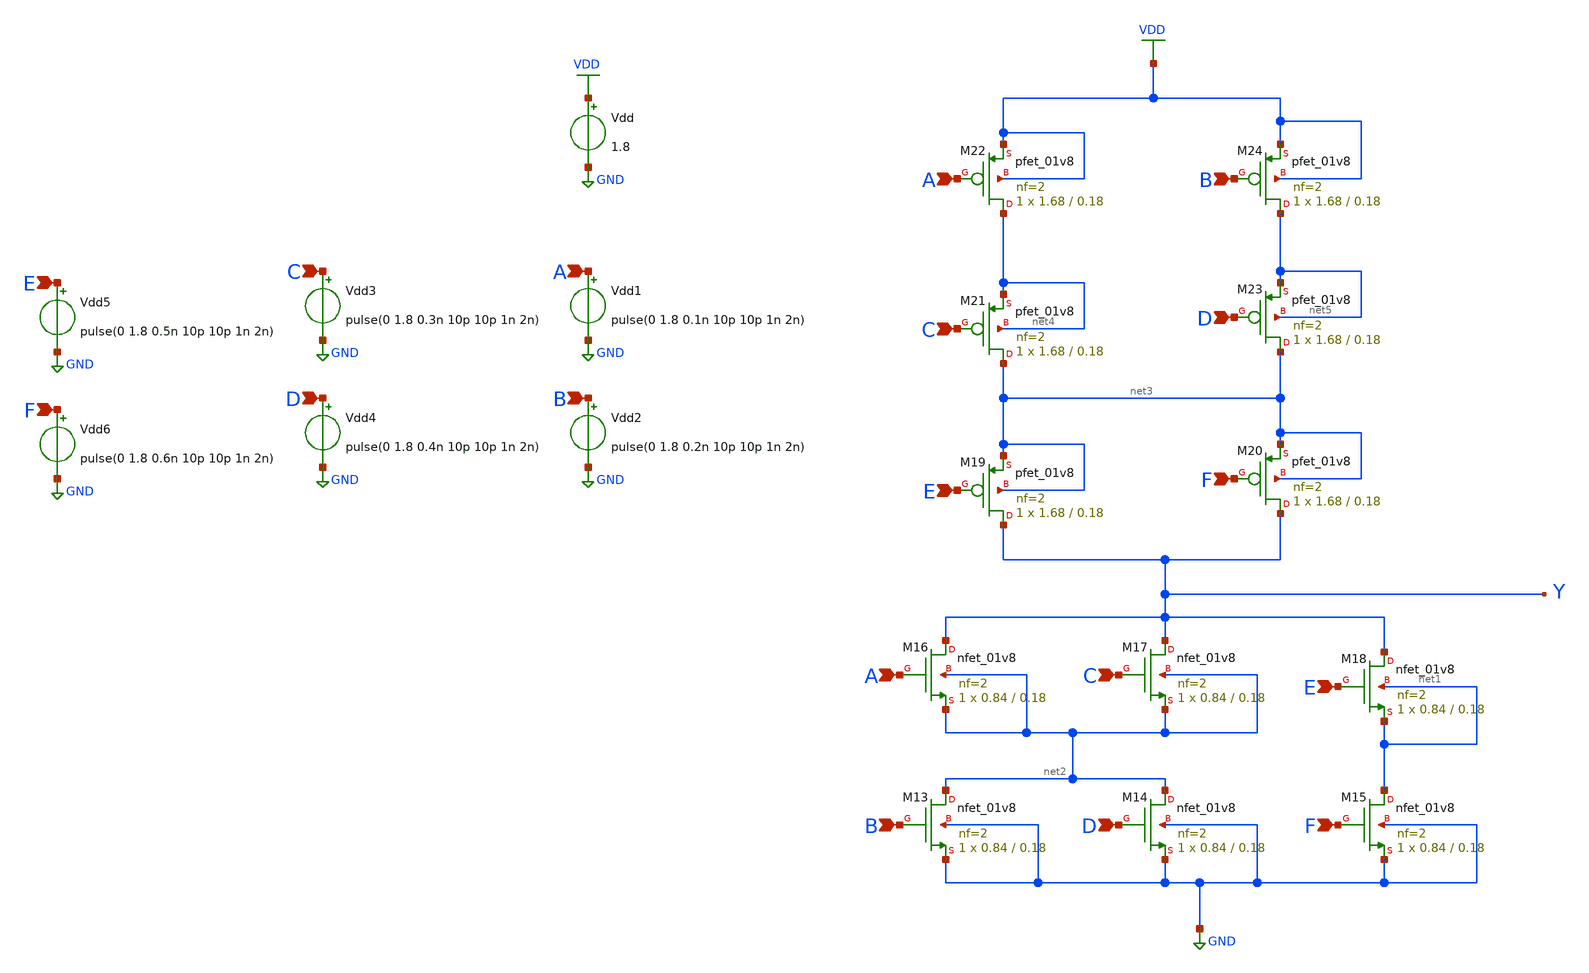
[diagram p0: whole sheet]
** sch_path: Week 1/xschem 840_1680/Function_Sky130.sch
**.subckt Function_Sky130 A B C D E F A C B D E F E F C D A B
*.ipin A
*.ipin B
*.ipin C
*.ipin D
*.ipin E
*.ipin F
*.ipin A
*.ipin C
*.ipin B
*.ipin D
*.ipin E
*.ipin F
*.ipin E
*.ipin F
*.ipin C
*.ipin D
*.ipin A
*.ipin B
Vdd VDD GND 1.8
Vdd1 A GND pulse(0 1.8 0.1n 10p 10p 1n 2n)
Vdd2 B GND pulse(0 1.8 0.2n 10p 10p 1n 2n)
Vdd3 C GND pulse(0 1.8 0.3n 10p 10p 1n 2n)
Vdd4 D GND pulse(0 1.8 0.4n 10p 10p 1n 2n)
Vdd5 E GND pulse(0 1.8 0.5n 10p 10p 1n 2n)
Vdd6 F GND pulse(0 1.8 0.6n 10p 10p 1n 2n)
XM13 net2 B GND GND sky130_fd_pr__nfet_01v8 L=0.18 W=0.84 nf=2 ad='int((nf+1)/2) * W/nf * 0.29' as='int((nf+2)/2) * W/nf * 0.29'
+ pd='2*int((nf+1)/2) * (W/nf + 0.29)' ps='2*int((nf+2)/2) * (W/nf + 0.29)' nrd='0.29 / W' nrs='0.29 / W'
+ sa=0 sb=0 sd=0 mult=1 m=1
XM14 net2 D GND GND sky130_fd_pr__nfet_01v8 L=0.18 W=0.84 nf=2 ad='int((nf+1)/2) * W/nf * 0.29' as='int((nf+2)/2) * W/nf * 0.29'
+ pd='2*int((nf+1)/2) * (W/nf + 0.29)' ps='2*int((nf+2)/2) * (W/nf + 0.29)' nrd='0.29 / W' nrs='0.29 / W'
+ sa=0 sb=0 sd=0 mult=1 m=1
XM15 net1 F GND GND sky130_fd_pr__nfet_01v8 L=0.18 W=0.84 nf=2 ad='int((nf+1)/2) * W/nf * 0.29' as='int((nf+2)/2) * W/nf * 0.29'
+ pd='2*int((nf+1)/2) * (W/nf + 0.29)' ps='2*int((nf+2)/2) * (W/nf + 0.29)' nrd='0.29 / W' nrs='0.29 / W'
+ sa=0 sb=0 sd=0 mult=1 m=1
XM16 Y A net2 net2 sky130_fd_pr__nfet_01v8 L=0.18 W=0.84 nf=2 ad='int((nf+1)/2) * W/nf * 0.29' as='int((nf+2)/2) * W/nf * 0.29'
+ pd='2*int((nf+1)/2) * (W/nf + 0.29)' ps='2*int((nf+2)/2) * (W/nf + 0.29)' nrd='0.29 / W' nrs='0.29 / W'
+ sa=0 sb=0 sd=0 mult=1 m=1
XM17 Y C net2 net2 sky130_fd_pr__nfet_01v8 L=0.18 W=0.84 nf=2 ad='int((nf+1)/2) * W/nf * 0.29' as='int((nf+2)/2) * W/nf * 0.29'
+ pd='2*int((nf+1)/2) * (W/nf + 0.29)' ps='2*int((nf+2)/2) * (W/nf + 0.29)' nrd='0.29 / W' nrs='0.29 / W'
+ sa=0 sb=0 sd=0 mult=1 m=1
XM18 Y E net1 net1 sky130_fd_pr__nfet_01v8 L=0.18 W=0.84 nf=2 ad='int((nf+1)/2) * W/nf * 0.29' as='int((nf+2)/2) * W/nf * 0.29'
+ pd='2*int((nf+1)/2) * (W/nf + 0.29)' ps='2*int((nf+2)/2) * (W/nf + 0.29)' nrd='0.29 / W' nrs='0.29 / W'
+ sa=0 sb=0 sd=0 mult=1 m=1
XM19 Y E net3 net3 sky130_fd_pr__pfet_01v8 L=0.18 W=1.68 nf=2 ad='int((nf+1)/2) * W/nf * 0.29' as='int((nf+2)/2) * W/nf * 0.29'
+ pd='2*int((nf+1)/2) * (W/nf + 0.29)' ps='2*int((nf+2)/2) * (W/nf + 0.29)' nrd='0.29 / W' nrs='0.29 / W'
+ sa=0 sb=0 sd=0 mult=1 m=1
XM20 Y F net3 net3 sky130_fd_pr__pfet_01v8 L=0.18 W=1.68 nf=2 ad='int((nf+1)/2) * W/nf * 0.29' as='int((nf+2)/2) * W/nf * 0.29'
+ pd='2*int((nf+1)/2) * (W/nf + 0.29)' ps='2*int((nf+2)/2) * (W/nf + 0.29)' nrd='0.29 / W' nrs='0.29 / W'
+ sa=0 sb=0 sd=0 mult=1 m=1
XM21 net3 C net4 net4 sky130_fd_pr__pfet_01v8 L=0.18 W=1.68 nf=2 ad='int((nf+1)/2) * W/nf * 0.29' as='int((nf+2)/2) * W/nf * 0.29'
+ pd='2*int((nf+1)/2) * (W/nf + 0.29)' ps='2*int((nf+2)/2) * (W/nf + 0.29)' nrd='0.29 / W' nrs='0.29 / W'
+ sa=0 sb=0 sd=0 mult=1 m=1
XM22 net4 A VDD VDD sky130_fd_pr__pfet_01v8 L=0.18 W=1.68 nf=2 ad='int((nf+1)/2) * W/nf * 0.29' as='int((nf+2)/2) * W/nf * 0.29'
+ pd='2*int((nf+1)/2) * (W/nf + 0.29)' ps='2*int((nf+2)/2) * (W/nf + 0.29)' nrd='0.29 / W' nrs='0.29 / W'
+ sa=0 sb=0 sd=0 mult=1 m=1
XM23 net3 D net5 net5 sky130_fd_pr__pfet_01v8 L=0.18 W=1.68 nf=2 ad='int((nf+1)/2) * W/nf * 0.29' as='int((nf+2)/2) * W/nf * 0.29'
+ pd='2*int((nf+1)/2) * (W/nf + 0.29)' ps='2*int((nf+2)/2) * (W/nf + 0.29)' nrd='0.29 / W' nrs='0.29 / W'
+ sa=0 sb=0 sd=0 mult=1 m=1
XM24 net5 B VDD VDD sky130_fd_pr__pfet_01v8 L=0.18 W=1.68 nf=2 ad='int((nf+1)/2) * W/nf * 0.29' as='int((nf+2)/2) * W/nf * 0.29'
+ pd='2*int((nf+1)/2) * (W/nf + 0.29)' ps='2*int((nf+2)/2) * (W/nf + 0.29)' nrd='0.29 / W' nrs='0.29 / W'
+ sa=0 sb=0 sd=0 mult=1 m=1
**** begin user architecture code


.lib ~/open_pdks/sources/sky130-pdk/libraries/sky130_fd_pr/latest/models/sky130.lib.spice tt
.control
save all
tran 10p 4n
plot y
.endc

**** end user architecture code
**.ends
.GLOBAL GND
.GLOBAL VDD
.end
